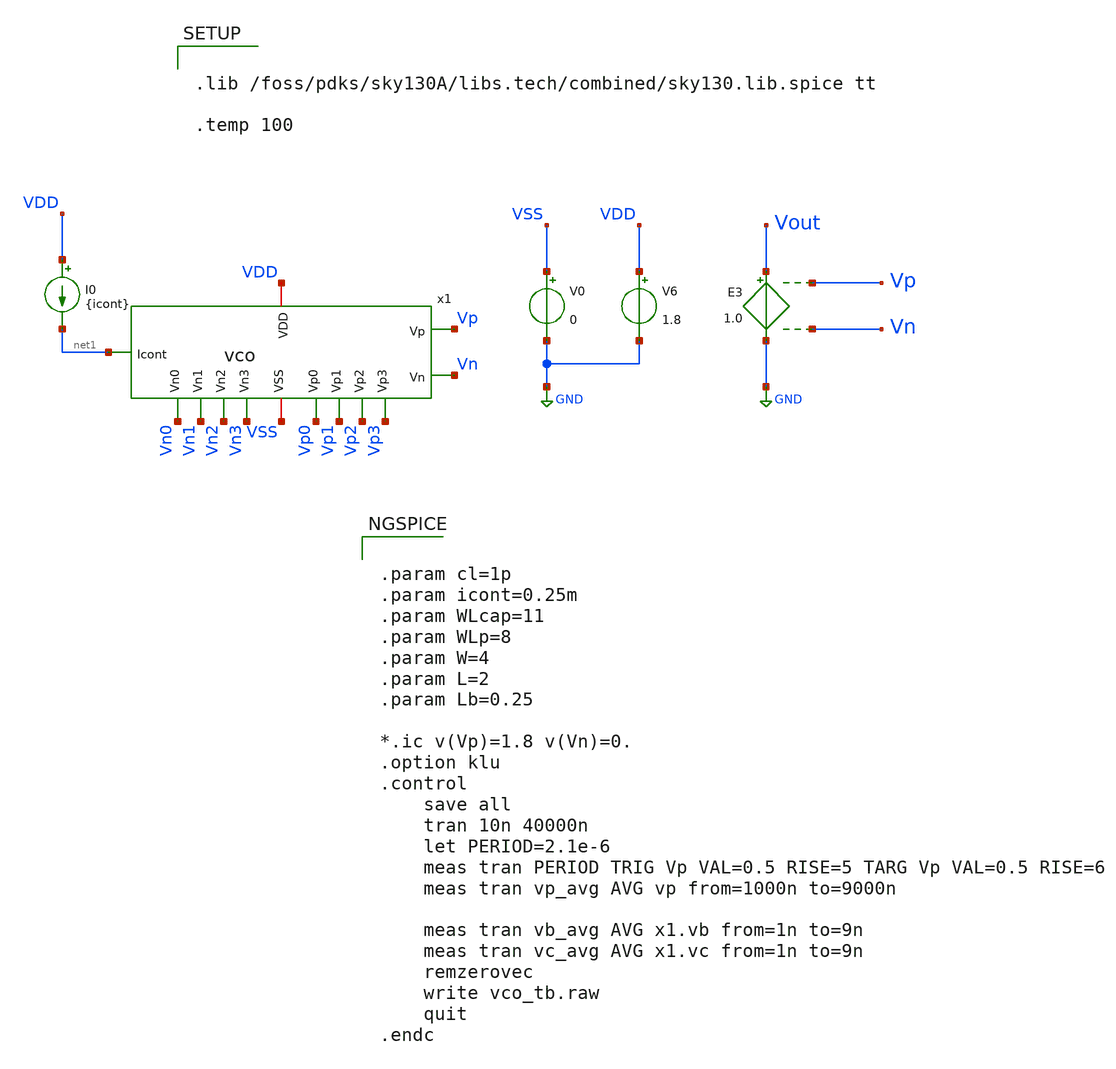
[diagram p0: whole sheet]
** sch_path: xschem/vco_tb.sch
**.subckt vco_tb
V0 VSS GND 0
V6 VDD GND 1.8
I0 VDD net1 {icont}
E3 Vout GND Vp Vn 1.0
x1 VDD VSS net1 Vp Vn Vp0 Vp1 Vp2 Vp3 Vn0 Vn1 Vn2 Vn3 vco
**** begin user architecture code


.param cl=1p
.param icont=0.25m
.param WLcap=11
.param WLp=8
.param W=4
.param L=2
.param Lb=0.25

*.ic v(Vp)=1.8 v(Vn)=0.
.option klu
.control
	save all
	tran 10n 40000n
	let PERIOD=2.1e-6
	meas tran PERIOD TRIG Vp VAL=0.5 RISE=5 TARG Vp VAL=0.5 RISE=6
	meas tran vp_avg AVG vp from=1000n to=9000n

	meas tran vb_avg AVG x1.vb from=1n to=9n
	meas tran vc_avg AVG x1.vc from=1n to=9n
	remzerovec
	write vco_tb.raw
	quit
.endc




.lib /foss/pdks/sky130A/libs.tech/combined/sky130.lib.spice tt

.temp 100


**** end user architecture code
**.ends
.GLOBAL GND
.end
